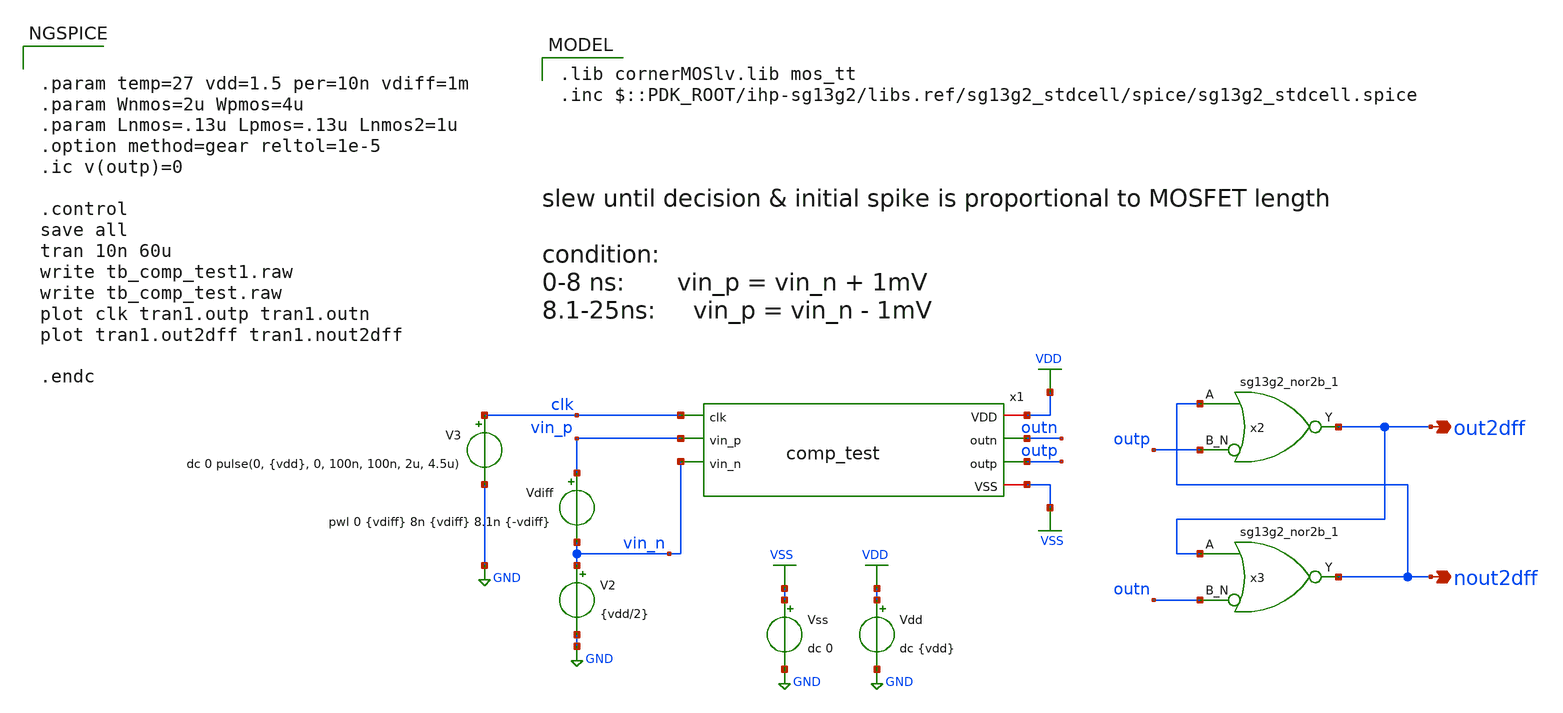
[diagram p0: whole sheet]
** sch_path: DSM/Schematics/new_comp/tb_comp_test.sch
**.subckt tb_comp_test out2dff nout2dff
*.opin out2dff
*.opin nout2dff
V2 vin_n GND {vdd/2}
V3 clk GND dc 0 pulse(0, {vdd}, 0, 100n, 100n, 2u, 4.5u)
Vdiff vin_p vin_n pwl 0 {vdiff} 8n {vdiff} 8.1n {-vdiff}
Vdd VDD GND dc {vdd}
Vss VSS GND dc 0
x2 out2dff nout2dff outp VDD VSS sg13g2_nor2b_1
x3 nout2dff out2dff outn VDD VSS sg13g2_nor2b_1
x1 VDD clk outn outp vin_p vin_n VSS comp_test
**** begin user architecture code
 .lib cornerMOSlv.lib mos_tt
.inc $::PDK_ROOT/ihp-sg13g2/libs.ref/sg13g2_stdcell/spice/sg13g2_stdcell.spice


.param temp=27 vdd=1.5 per=10n vdiff=1m
.param Wnmos=2u Wpmos=4u
.param Lnmos=.13u Lpmos=.13u Lnmos2=1u
.option method=gear reltol=1e-5
.ic v(outp)=0

.control
save all
tran 10n 60u
write tb_comp_test1.raw
write tb_comp_test.raw
plot clk tran1.outp tran1.outn
plot tran1.out2dff tran1.nout2dff

.endc

**** end user architecture code
**.ends
.GLOBAL GND
.GLOBAL VDD
.GLOBAL VSS
.end
